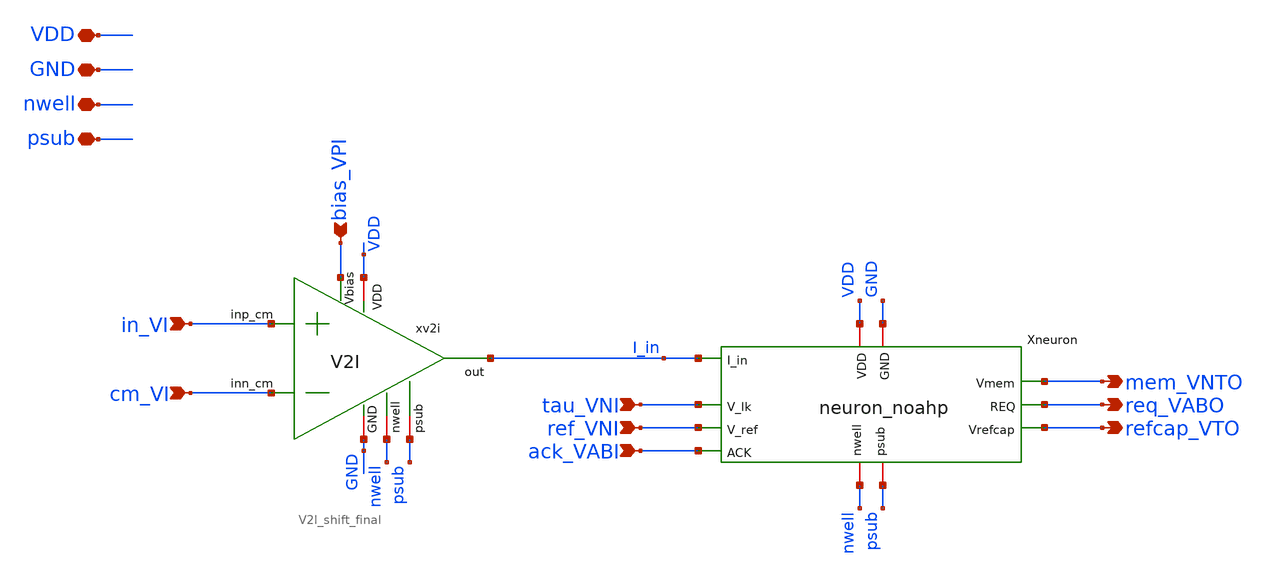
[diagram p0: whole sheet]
** sch_path: xschem/neuron_row.sch
**.subckt neuron_row in_VI cm_VI bias_VPI VDD GND nwell psub mem_VNTO req_VABO refcap_VTO tau_VNI
*+ ref_VNI ack_VABI
*.ipin in_VI
*.ipin cm_VI
*.ipin bias_VPI
*.iopin VDD
*.iopin GND
*.iopin nwell
*.iopin psub
*.opin mem_VNTO
*.opin req_VABO
*.opin refcap_VTO
*.ipin tau_VNI
*.ipin ref_VNI
*.ipin ack_VABI
Xneuron VDD I_in tau_VNI mem_VNTO req_VABO ack_VABI ref_VNI GND refcap_VTO psub nwell neuron_noahp
xv2i VDD bias_VPI cm_VI in_VI I_in GND nwell psub V2I_shift_final
**.ends

* expanding   symbol:  neuron_noahp.sym # of pins=11
** sym_path: xschem/neuron_noahp.sym
** sch_path: xschem/neuron_noahp.sch
.subckt neuron_noahp VDD I_in V_lk Vmem REQ ACK V_ref GND Vrefcap psub nwell
*.ipin V_ref
*.iopin GND
*.iopin VDD
*.opin REQ
*.ipin ACK
*.ipin I_in
*.ipin V_lk
*.opin Vmem
*.opin Vrefcap
*.iopin psub
*.iopin nwell
Xinv1 VDD nwell net1 Vfb psub GND inv
Xinv2 VDD nwell REQ net1 psub GND inv
Xdpi1 I_in VDD Vmem V_lk GND nwell psub DPI
Xfb VDD Vfb Vmem GND nwell psub FB_system
Xref ACK Vmem REQ Vrefcap GND V_ref VDD nwell psub REF_system
XCmem Vmem GND cap_cmim w=44.4e-6 l=15e-6 m=1 mm_ok=1
XCref Vrefcap GND cap_cmim w=22.1e-6 l=15e-6 m=1 mm_ok=1
.ends


* expanding   symbol:  V2I_shift_final.sym # of pins=8
** sym_path: xschem/V2I_shift_final.sym
** sch_path: xschem/V2I_shift_final.sch
.subckt V2I_shift_final VDD Vbias inn_cm inp_cm out GND nwell psub
*.ipin inn_cm
*.ipin inp_cm
*.opin out
*.ipin Vbias
*.iopin VDD
*.iopin GND
*.iopin psub
*.iopin nwell
XMIRA Vm Vm GND psub sg13_hv_nmos w=4u l=1u ng=2 m=4 mm_ok=1
XMBIAS Vb Vbias VDD nwell sg13_hv_pmos w=4u l=1u ng=2 m=4 mm_ok=1
XMIRB out Vm GND psub sg13_hv_nmos w=4u l=1u ng=2 m=4 mm_ok=1
XMdiffINN out inn_cm Vb nwell sg13_hv_pmos w=4u l=1u ng=2 m=4 mm_ok=1
XMDBIAS VDD VDD VDD nwell sg13_hv_pmos w=4u l=1u ng=2 m=2 mm_ok=1
XMIDC out Vbias VDD nwell sg13_hv_pmos w=3u l=1u ng=2 m=4 mm_ok=1
XMDIDC VDD VDD VDD nwell sg13_hv_pmos w=3u l=1u ng=2 m=2 mm_ok=1
XMdiffINP Vm inp_cm Vb nwell sg13_hv_pmos w=4u l=1u ng=2 m=4 mm_ok=1
XMDdiffINP Vb Vb Vb nwell sg13_hv_pmos w=4u l=1u ng=2 m=2 mm_ok=1
XMDdiffINN Vb Vb Vb nwell sg13_hv_pmos w=4u l=1u ng=2 m=2 mm_ok=1
XMDNMIRA GND GND GND psub sg13_hv_nmos w=4u l=1u ng=2 m=2 mm_ok=1
XMDNMIRB GND GND GND psub sg13_hv_nmos w=4u l=1u ng=2 m=2 mm_ok=1
XR3 GND psub ptap1 R=4.709 w=18.5e-6 l=6.3e-6 rw=0.3e-6
XR1 VDD nwell ntap1 R=3.606 w=19.5e-6 l=12.7e-6 rw=0.3e-6
.ends


* expanding   symbol:  inv.sym # of pins=6
** sym_path: xschem/inv.sym
** sch_path: xschem/inv.sch
.subckt inv VDD nwell out in psub GND
*.ipin in
*.iopin GND
*.opin out
*.iopin VDD
*.iopin nwell
*.iopin psub
XM1 out in VDD nwell sg13_hv_pmos w=4u l=0.5u ng=1 m=1 mm_ok=1
XM2 out in GND psub sg13_hv_nmos w=4u l=0.5u ng=1 m=1 mm_ok=1
XR1 GND psub ptap1 R=122.5 w=2e-6 l=1e-6
XR2 VDD nwell ntap1 R=122.5 w=2e-6 l=1e-6
.ends


* expanding   symbol:  DPI.sym # of pins=7
** sym_path: xschem/DPI.sym
** sch_path: xschem/DPI.sch
.subckt DPI I_in VDD V_mem V_lk GND nwell psub
*.opin V_mem
*.ipin V_lk
*.ipin I_in
*.iopin VDD
*.iopin GND
*.iopin nwell
*.iopin psub
XMdifl GND V_lk I_in nwell sg13_hv_pmos w=2u l=2u ng=2 m=8 mm_ok=1
XMdifr V_mem V_mem I_in nwell sg13_hv_pmos w=2u l=2u ng=2 m=8 mm_ok=1
XMtau V_mem V_lk GND psub sg13_hv_nmos w=4u l=4u ng=2 m=4 mm_ok=1
XR1 VDD nwell ntap1 R=16.73 w=25.2e-6 l=0.3e-6
XR2 VDD nwell ntap1 R=46.01 w=0.3e-6 l=9e-6
XR3 VDD nwell ntap1 R=46.01 w=0.3e-6 l=9e-6
XR4 GND psub ptap1 R=3.342 w=25.7e-6 l=9e-6 rw=0.3e-6
XMdum1 VDD VDD VDD nwell sg13_hv_pmos w=5u l=2u ng=10 m=2 mm_ok=1
XMdum2 I_in VDD VDD nwell sg13_hv_pmos w=1u l=2u ng=1 m=8 mm_ok=1
XMdum3 GND GND GND psub sg13_hv_nmos w=2u l=4u ng=4 m=2 mm_ok=1
XMdum4 GND GND GND psub sg13_hv_nmos w=0.5u l=3u ng=1 m=4 mm_ok=1
XMdum5 GND GND GND psub sg13_hv_nmos w=2u l=3u ng=1 m=4 mm_ok=1
.ends


* expanding   symbol:  FB_system.sym # of pins=6
** sym_path: xschem/FB_system.sym
** sch_path: xschem/FB_system.sch
.subckt FB_system VDD out V_mem GND nwell psub
*.opin out
*.iopin V_mem
*.iopin VDD
*.iopin GND
*.iopin nwell
*.iopin psub
XMmirr Vmir Vmir VDD nwell sg13_hv_pmos w=4u l=2u ng=4 m=1 mm_ok=1
XMmirl4 V_mem Vmir net1 nwell sg13_hv_pmos w=1u l=2u ng=1 m=1 mm_ok=1
XMthr out V_mem Vmir nwell sg13_hv_pmos w=4u l=2u ng=4 m=1 mm_ok=1
XMmem1 out V_mem net2 psub sg13_hv_nmos w=1u l=2u ng=1 m=2 mm_ok=1
XMmirl3 net1 Vmir net3 nwell sg13_hv_pmos w=1u l=2u ng=1 m=1 mm_ok=1
XMmirl2 net3 Vmir net4 nwell sg13_hv_pmos w=1u l=2u ng=1 m=1 mm_ok=1
XMmirl1 net4 Vmir VDD nwell sg13_hv_pmos w=1u l=2u ng=1 m=1 mm_ok=1
XMmem2 net2 V_mem net5 psub sg13_hv_nmos w=1u l=2u ng=1 m=2 mm_ok=1
XMmem3 net5 V_mem net6 psub sg13_hv_nmos w=1u l=2u ng=1 m=2 mm_ok=1
XMmem4 net6 V_mem GND psub sg13_hv_nmos w=1u l=2u ng=1 m=2 mm_ok=1
XMdum1 GND GND GND psub sg13_hv_nmos w=6u l=2u ng=6 m=2 mm_ok=1
XMdum2 GND GND GND psub sg13_hv_nmos w=1u l=2u ng=1 m=2 mm_ok=1
XMdum3 out GND GND psub sg13_hv_nmos w=1u l=2u ng=1 m=2 mm_ok=1
XMdum4 VDD VDD VDD nwell sg13_hv_pmos w=6u l=2u ng=6 m=2 mm_ok=1
XMdum5 VDD VDD VDD nwell sg13_hv_pmos w=1u l=2u ng=1 m=3 mm_ok=1
XMdum6 out VDD VDD nwell sg13_hv_pmos w=1u l=2u ng=1 m=2 mm_ok=1
XMdum7 V_mem VDD VDD nwell sg13_hv_pmos w=1u l=2u ng=1 m=1 mm_ok=1
.ends


* expanding   symbol:  REF_system.sym # of pins=9
** sym_path: xschem/REF_system.sym
** sch_path: xschem/REF_system.sch
.subckt REF_system ACK V_mem REQ Vrefcap GND V_ref VDD nwell psub
*.iopin VDD
*.iopin GND
*.ipin V_ref
*.ipin REQ
*.ipin ACK
*.ipin V_mem
*.opin Vrefcap
*.iopin psub
*.iopin nwell
XM10 Vrefcap REQ net2 nwell sg13_hv_pmos w=1u l=0.5u ng=1 m=1 mm_ok=1
XM11 Vrefcap REQ net1 psub sg13_hv_nmos w=1u l=0.5u ng=1 m=1 mm_ok=1
XM12 net2 ACK VDD nwell sg13_hv_pmos w=1u l=0.5u ng=1 m=1 mm_ok=1
XM13 V_mem Vrefcap GND psub sg13_hv_nmos w=1u l=0.5u ng=1 m=1 mm_ok=1
XM14 net1 V_ref GND psub sg13_hv_nmos w=4u l=4u ng=2 m=4 mm_ok=1
XMdum3 GND GND GND psub sg13_hv_nmos w=2u l=4u ng=4 m=2 mm_ok=1
XMdum4 GND GND GND psub sg13_hv_nmos w=0.5u l=3u ng=1 m=4 mm_ok=1
XMdum5 GND GND GND psub sg13_hv_nmos w=2u l=3u ng=1 m=4 mm_ok=1
XR4 GND psub ptap1 R=3.342 w=25.7e-6 l=9e-6 rw=0.3e-6
XR1 VDD nwell ntap1 R=3.748 w=24e-6 l=7e-6 rw=0.3e-6
.ends

.end
